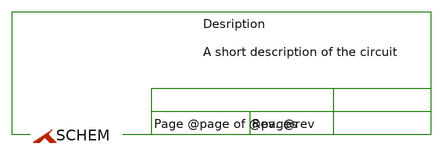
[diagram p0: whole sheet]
** sch_path: macros/_templates/template.sch
* Copyright (C) 1998-2024 Stefan Frederik Schippers
* This program is free software; you can redistribute it and/or modify
* it under the terms of the GNU General Public License as published by
* the Free Software Foundation; either version 2 of the License, or
* (at your option) any later version.
* This program is distributed in the hope that it will be useful,
* but WITHOUT ANY WARRANTY; without even the implied warranty of
* MERCHANTABILITY or FITNESS FOR A PARTICULAR PURPOSE.  See the
* GNU General Public License for more details.
* You should have received a copy of the GNU General Public License
* along with this program; if not, write to the Free Software
**.subckt template
**** begin user architecture code


.lib $::SG13G2_MODELS_XYCE/cornerMOSlv.lib mos_tt
.lib $::SG13G2_MODELS_XYCE/cornerMOShv.lib mos_tt
.lib $::SG13G2_MODELS_XYCE/cornerHBT.lib hbt_typ
.lib $::SG13G2_MODELS_XYCE/cornerRES.lib res_typ
.lib $::SG13G2_MODELS_XYCE/cornerDIO.lib dio_typ




.temp 27
.param vin=0




.lib cornerMOSlv.lib mos_tt
.lib cornerMOShv.lib mos_tt
.lib cornerHBT.lib hbt_typ
.lib cornerRES.lib res_typ
.lib cornerDIO.lib dio_tt




.preprocess replaceground true
.option temp=27
.op


**** end user architecture code
**.ends
.end
